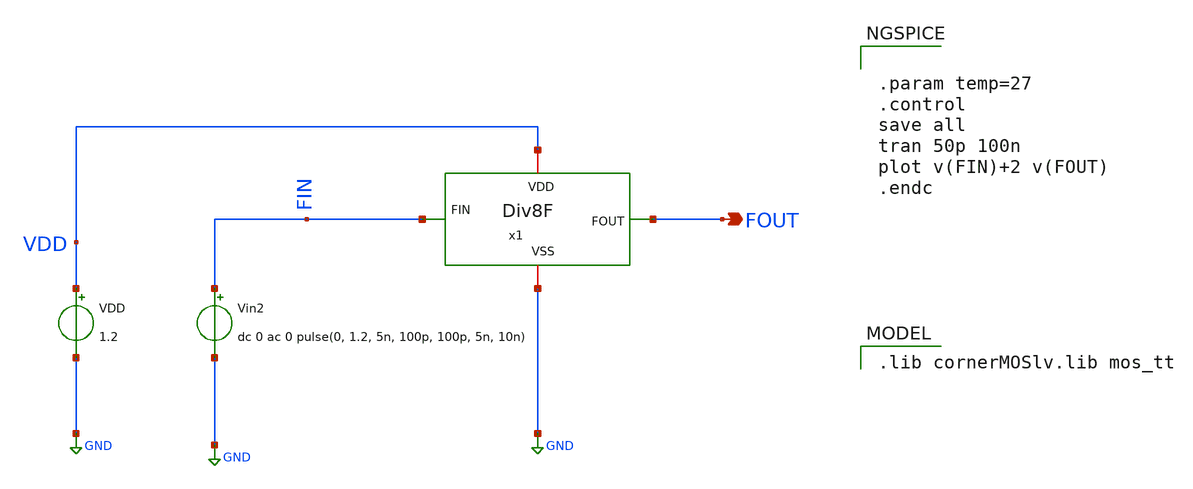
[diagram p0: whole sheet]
** sch_path: Team Designs/Team 1 Design/design_data/xschem/FD(Frequency_Dividers)/Div8F/Div8F_tb.sch
**.subckt Div8F_tb FOUT
*.opin FOUT
VDD VDD GND 1.2
Vin2 FIN GND dc 0 ac 0 pulse(0, 1.2, 5n, 100p, 100p, 5n, 10n)
x1 VDD FOUT FIN GND Div8F
**** begin user architecture code
 .lib cornerMOSlv.lib mos_tt



.param temp=27
.control
save all
tran 50p 100n
plot v(FIN)+2 v(FOUT)
.endc


**** end user architecture code
**.ends
.GLOBAL GND
.end
